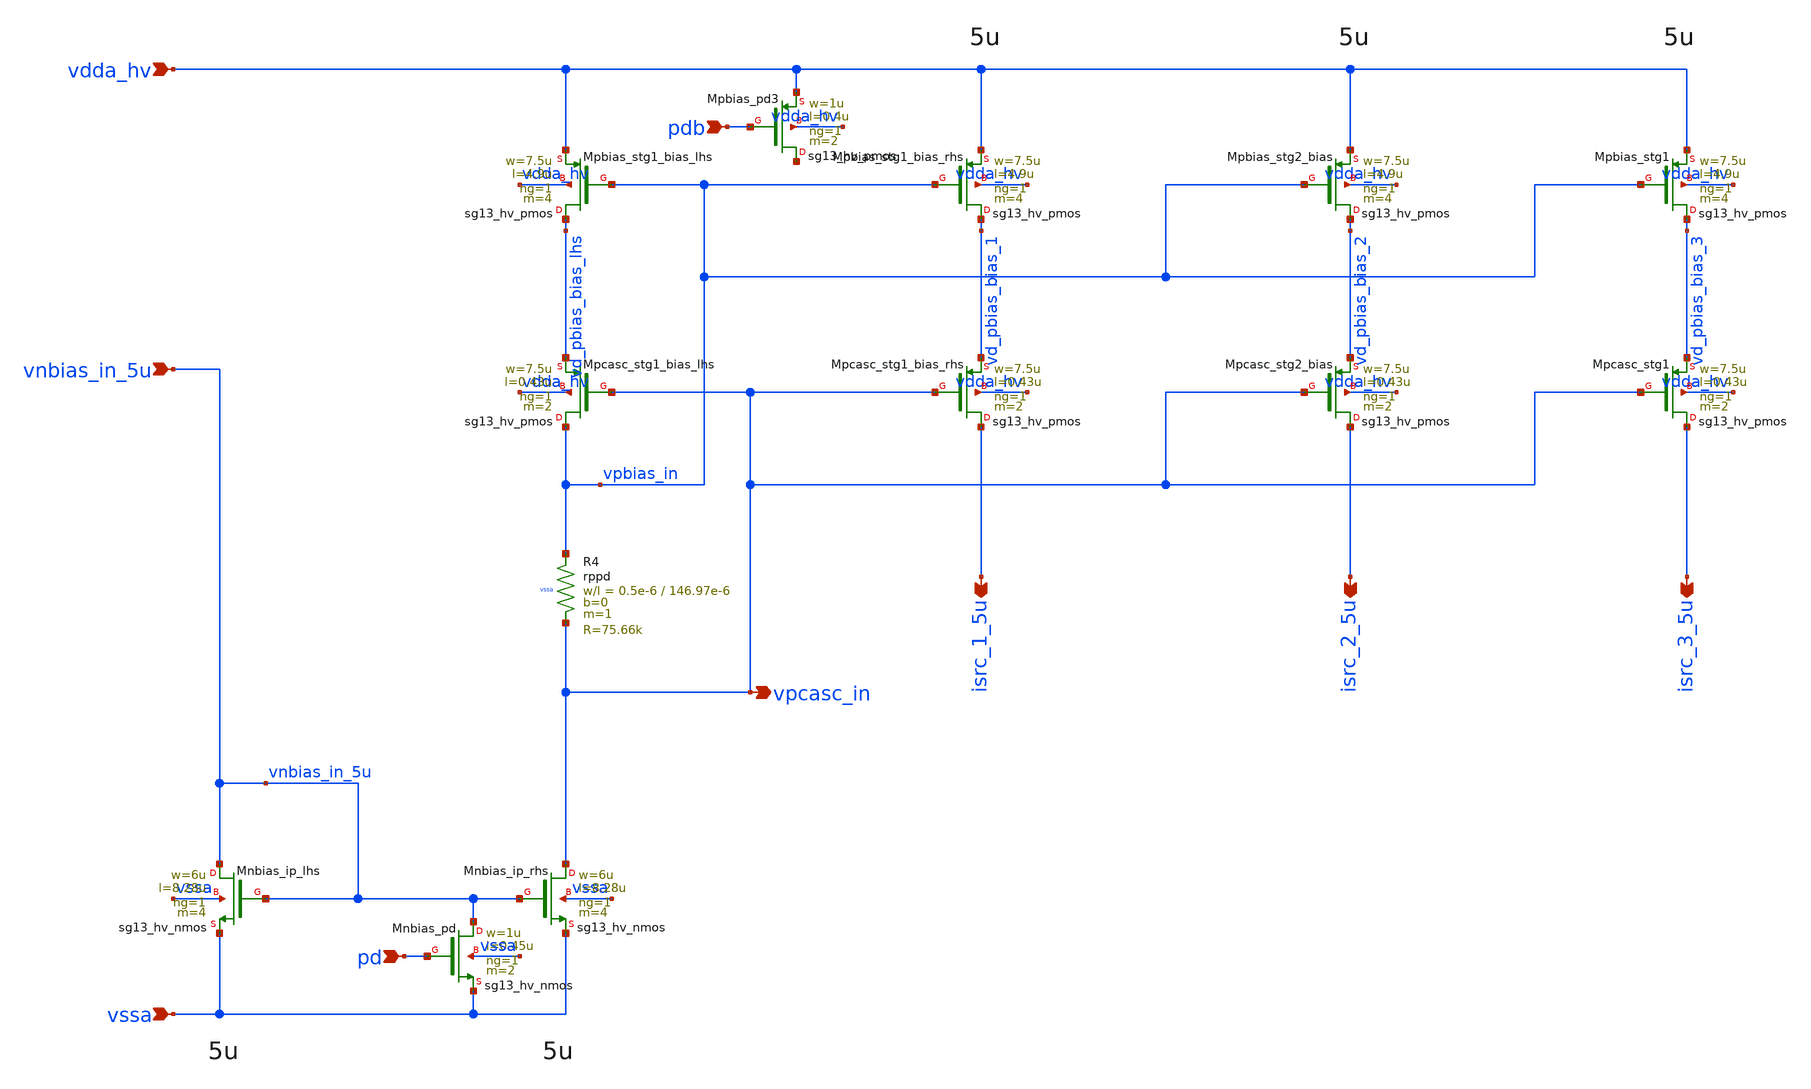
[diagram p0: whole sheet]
** sch_path: Schematics_Layout/sunrise_opamp_bias/sunrise_opamp_bias.sch
**.subckt sunrise_opamp_bias vdda_hv vssa vnbias_in_5u pd pdb vpcasc_in isrc_1_5u isrc_2_5u
*+ isrc_3_5u
*.ipin vdda_hv
*.ipin vssa
*.ipin vnbias_in_5u
*.ipin pd
*.ipin pdb
*.opin vpcasc_in
*.opin isrc_1_5u
*.opin isrc_2_5u
*.opin isrc_3_5u
XMnbias_ip_lhs vnbias_in_5u vnbias_in_5u vssa vssa sg13_hv_nmos w=6u l=8.28u ng=1 m=4 mm_ok=1
XMnbias_ip_rhs vpcasc_in vnbias_in_5u vssa vssa sg13_hv_nmos w=6u l=8.28u ng=1 m=4 mm_ok=1
XMpcasc_stg1_bias_lhs vpbias_in vpcasc_in vd_pbias_bias_lhs vdda_hv sg13_hv_pmos w=7.5u l=0.43u ng=1
+ m=2 mm_ok=1
XMpbias_stg1_bias_lhs vd_pbias_bias_lhs vpbias_in vdda_hv vdda_hv sg13_hv_pmos w=7.5u l=4.9u ng=1
+ m=4 mm_ok=1
XMpcasc_stg1_bias_rhs isrc_1_5u vpcasc_in vd_pbias_bias_1 vdda_hv sg13_hv_pmos w=7.5u l=0.43u ng=1
+ m=2 mm_ok=1
XMpbias_stg1_bias_rhs vd_pbias_bias_1 vpbias_in vdda_hv vdda_hv sg13_hv_pmos w=7.5u l=4.9u ng=1 m=4
+ mm_ok=1
XMpcasc_stg2_bias isrc_2_5u vpcasc_in vd_pbias_bias_2 vdda_hv sg13_hv_pmos w=7.5u l=0.43u ng=1 m=2
+ mm_ok=1
XMpbias_stg2_bias vd_pbias_bias_2 vpbias_in vdda_hv vdda_hv sg13_hv_pmos w=7.5u l=4.9u ng=1 m=4
+ mm_ok=1
XR4 vpbias_in vpcasc_in vssa rppd w=0.5e-6 l=146.97e-6 m=1 b=0 mm_ok=1
XMnbias_pd vnbias_in_5u pd vssa vssa sg13_hv_nmos w=1u l=0.45u ng=1 m=2 mm_ok=1
XMpbias_pd3 net1 pdb vdda_hv vdda_hv sg13_hv_pmos w=1u l=0.4u ng=1 m=2 mm_ok=1
XMpcasc_stg1 isrc_3_5u vpcasc_in vd_pbias_bias_3 vdda_hv sg13_hv_pmos w=7.5u l=0.43u ng=1 m=2
+ mm_ok=1
XMpbias_stg1 vd_pbias_bias_3 vpbias_in vdda_hv vdda_hv sg13_hv_pmos w=7.5u l=4.9u ng=1 m=4 mm_ok=1
**.ends
.end
